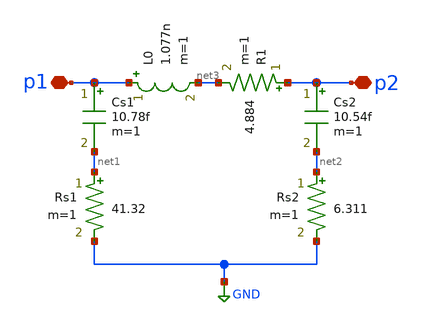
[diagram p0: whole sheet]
** sch_path: ask_modulator/xschem/l0.sch
**.subckt l0 p2 p1
*.iopin p2
*.iopin p1
L0 p1 net3 1.077n m=1
Cs1 p1 net1 10.78f m=1
Cs2 p2 net2 10.54f m=1
Rs1 net1 GND 41.32 m=1
Rs2 net2 GND 6.311 m=1
R1 p2 net3 4.884 m=1
**.ends
.GLOBAL GND
.end
